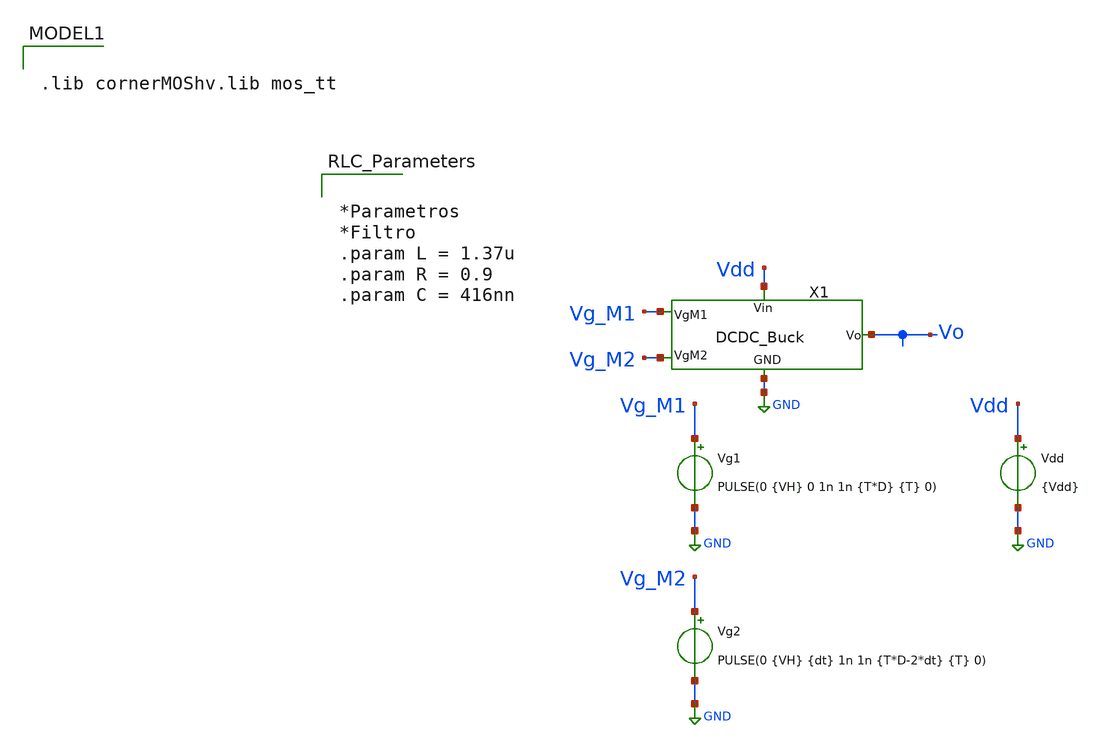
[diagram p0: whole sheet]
** sch_path: xschem/TB_DCDCBuck.sch
**.subckt TB_DCDCBuck
X1 Vg_M1 Vg_M2 Vdd net1 Vo DCDC_Buck
Vdd Vdd GND {Vdd}
Vg2 Vg_M2 GND PULSE(0 {VH} {dt} 1n 1n {T*D-2*dt} {T} 0)
Vg1 Vg_M1 GND PULSE(0 {VH} 0 1n 1n {T*D} {T} 0)
**** begin user architecture code


.param temp=27
*.param mult_M1 = 2400
.param mult_M1 = 3600
.param w_M1 =10u
*.param l_M1 = 0.2u ** Posee mayor capacidad de corriente, pero en sub-umbral conduce mucha
*+ corriente
.param l_M1 = 0.22u
.param ng_M1 = 1

*.param mult_M2 = 1200
.param mult_M2 = 1800
.param w_M2 =10u
*.param l_M2 =0.25u
.param l_M2 =0.25u
.param ng_M2 =1







.param Vdd = 3.3
.param VH = 3.3
.param D = 0.42
.param T = 1u
.param dt = 0.1u
*.param dt = 400p
*.param dt = 600p
.param temp = 27






.save all


.control
reset
set color0 = white
tran 1n 20u
let Io = i(v.x1.V_Io)
let Po = Io*v(Vo)
meas tran Vo_mean AVG v(Vo) from=10u to=20u
meas tran Io_mean AVG Io from=10u to=20u
meas tran Po_mean AVG Po from=10u to=20u
plot Io i(v.x1.V_IL)
plot v(Vo)
plot Po
plot v(x1.Vc)
plot v(Vg_M1) v(Vg_M2)
.endc



.end



.lib cornerMOShv.lib mos_tt



*Parametros
*Filtro
.param L = 1.37u
.param R = 0.9
.param C = 416nn



**** end user architecture code
**.ends

* expanding   symbol:
*+  /workspaces/usm-vlsi-tools/shared_xserver/simulations/IHP-sg13g2/Simulaciones/Modulos/DCDC_Buck.sym # of pins=5
** sym_path: xschem/Modulos/DCDC_Buck.sym
** sch_path: xschem/Modulos/DCDC_Buck.sch
.subckt DCDC_Buck VgM1 VgM2 Vin GND Vo
*.iopin Vin
*.ipin VgM1
*.ipin VgM2
*.iopin Vo
*.iopin GND
XM2 GND VgM2 Vc GND sg13_hv_nmos w={w_M2} l={l_M2} ng={ng_M2} m={mult_M2} mm_ok=1
XM1 Vc VgM1 Vin Vin sg13_hv_pmos w={w_M1} l={l_M1} ng={ng_M1} m={mult_M1} mm_ok=1
L1 net2 net1 {L} m=1
C1 net1 GND {C} m=1
V_Io net1 Vo 0
.save i(v_io)
V_IL Vc net2 0
.save i(v_il)
R1 Vo GND {R} m=1
.ends

.GLOBAL GND
.end
